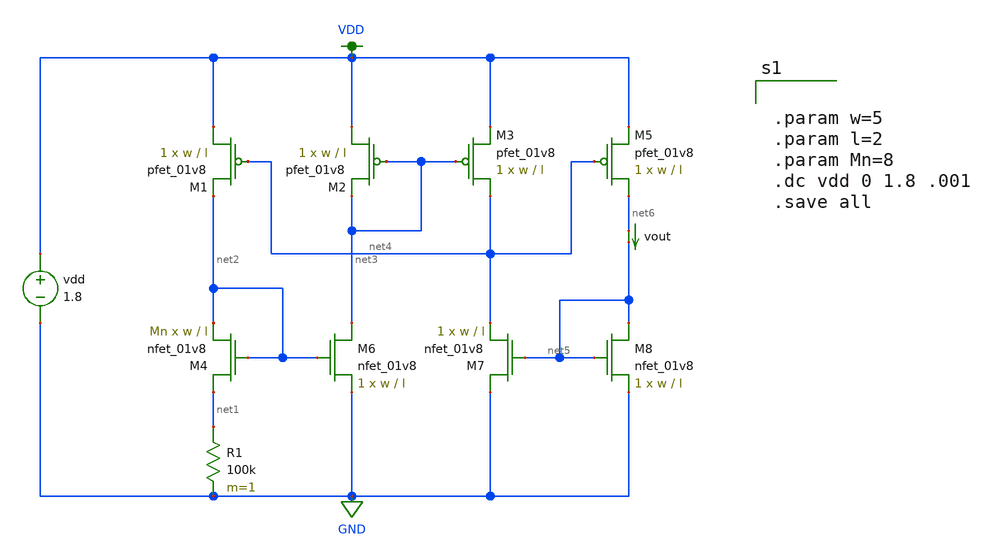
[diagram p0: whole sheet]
** sch_path: schematic/bias_current_resistive.sch
**.subckt bias_current_resistive
XM1 VDD net4 net2 VDD sky130_fd_pr__pfet_01v8 L=l W=w nf=1 ad='int((nf+1)/2) * W/nf * 0.29' as='int((nf+2)/2) * W/nf * 0.29'
+ pd='2*int((nf+1)/2) * (W/nf + 0.29)' ps='2*int((nf+2)/2) * (W/nf + 0.29)' nrd='0.29 / W' nrs='0.29 / W'
+ sa=0 sb=0 sd=0 mult=1 m=1
XM2 VDD net3 net3 VDD sky130_fd_pr__pfet_01v8 L=l W=w nf=1 ad='int((nf+1)/2) * W/nf * 0.29' as='int((nf+2)/2) * W/nf * 0.29'
+ pd='2*int((nf+1)/2) * (W/nf + 0.29)' ps='2*int((nf+2)/2) * (W/nf + 0.29)' nrd='0.29 / W' nrs='0.29 / W'
+ sa=0 sb=0 sd=0 mult=1 m=1
XM3 net4 net3 VDD VDD sky130_fd_pr__pfet_01v8 L=l W=w nf=1 ad='int((nf+1)/2) * W/nf * 0.29' as='int((nf+2)/2) * W/nf * 0.29'
+ pd='2*int((nf+1)/2) * (W/nf + 0.29)' ps='2*int((nf+2)/2) * (W/nf + 0.29)' nrd='0.29 / W' nrs='0.29 / W'
+ sa=0 sb=0 sd=0 mult=1 m=1
XM5 net6 net4 VDD VDD sky130_fd_pr__pfet_01v8 L=l W=w nf=1 ad='int((nf+1)/2) * W/nf * 0.29' as='int((nf+2)/2) * W/nf * 0.29'
+ pd='2*int((nf+1)/2) * (W/nf + 0.29)' ps='2*int((nf+2)/2) * (W/nf + 0.29)' nrd='0.29 / W' nrs='0.29 / W'
+ sa=0 sb=0 sd=0 mult=1 m=1
XM4 net1 net2 net2 GND sky130_fd_pr__nfet_01v8 L=l W=w nf=1 ad='int((nf+1)/2) * W/nf * 0.29' as='int((nf+2)/2) * W/nf * 0.29'
+ pd='2*int((nf+1)/2) * (W/nf + 0.29)' ps='2*int((nf+2)/2) * (W/nf + 0.29)' nrd='0.29 / W' nrs='0.29 / W'
+ sa=0 sb=0 sd=0 mult=Mn m=Mn
XM6 net3 net2 GND GND sky130_fd_pr__nfet_01v8 L=l W=w nf=1 ad='int((nf+1)/2) * W/nf * 0.29' as='int((nf+2)/2) * W/nf * 0.29'
+ pd='2*int((nf+1)/2) * (W/nf + 0.29)' ps='2*int((nf+2)/2) * (W/nf + 0.29)' nrd='0.29 / W' nrs='0.29 / W'
+ sa=0 sb=0 sd=0 mult=1 m=1
XM7 GND net5 net4 GND sky130_fd_pr__nfet_01v8 L=l W=w nf=1 ad='int((nf+1)/2) * W/nf * 0.29' as='int((nf+2)/2) * W/nf * 0.29'
+ pd='2*int((nf+1)/2) * (W/nf + 0.29)' ps='2*int((nf+2)/2) * (W/nf + 0.29)' nrd='0.29 / W' nrs='0.29 / W'
+ sa=0 sb=0 sd=0 mult=1 m=1
XM8 net5 net5 GND GND sky130_fd_pr__nfet_01v8 L=l W=w nf=1 ad='int((nf+1)/2) * W/nf * 0.29' as='int((nf+2)/2) * W/nf * 0.29'
+ pd='2*int((nf+1)/2) * (W/nf + 0.29)' ps='2*int((nf+2)/2) * (W/nf + 0.29)' nrd='0.29 / W' nrs='0.29 / W'
+ sa=0 sb=0 sd=0 mult=1 m=1
R1 net1 GND 100k m=1
vout net6 net5 0
.save i(vout)
vdd VDD GND 1.8
**** begin user architecture code


.param w=5
.param l=2
.param Mn=8
.dc vdd 0 1.8 .001
.save all



.option wnflag=1
.param MC_SWITCH=0.0
.lib ~/skywater/skywater-pdk/libraries/sky130_fd_pr_ngspice/latest/models/sky130.lib.spice tt

**** end user architecture code
**.ends
.GLOBAL GND
.GLOBAL VDD
.end
